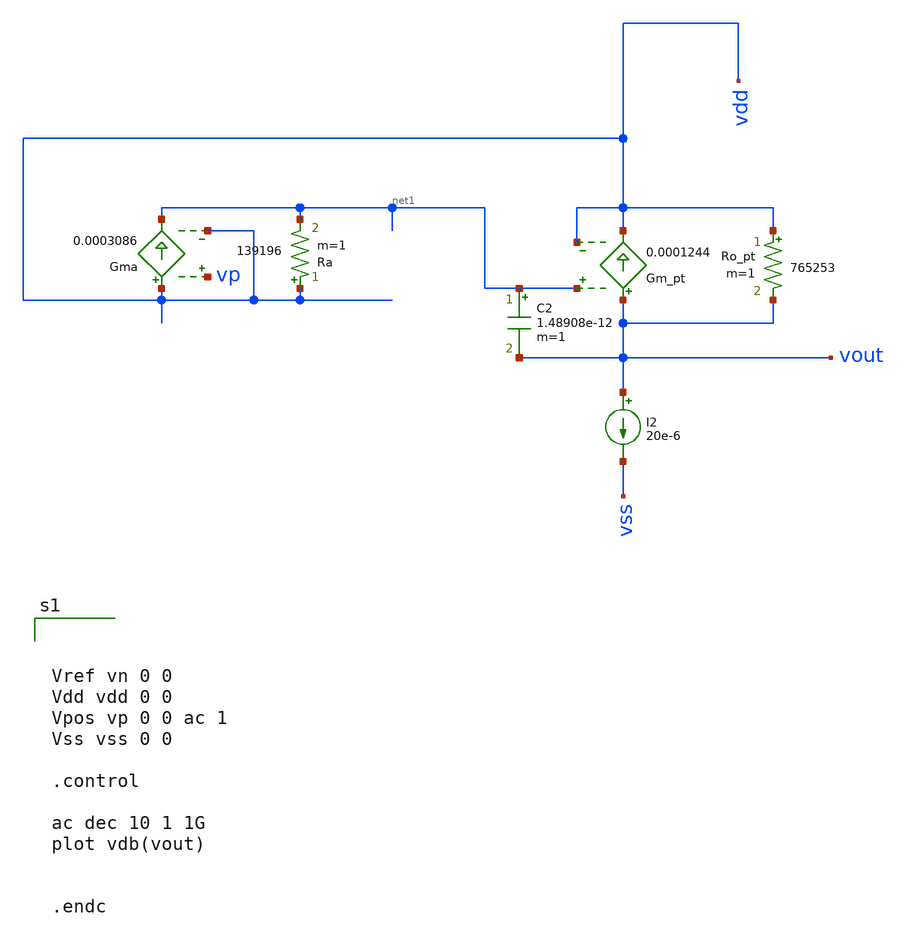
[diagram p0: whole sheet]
** sch_path: test/sstadex/xschem/stage2_OTA_tb.sch
**.subckt stage2_OTA_tb
Ro_pt vdd vout 765253 m=1
Gm_pt vout vdd net1 vdd 0.0001244
Gma vdd net1 vp vdd 0.0003086
Ra vdd net1 139196 m=1
I2 vout vss 20e-6
C2 net1 vout 1.48908e-12 m=1
**** begin user architecture code



Vref vn 0 0
Vdd vdd 0 0
Vpos vp 0 0 ac 1
Vss vss 0 0

.control

ac dec 10 1 1G
plot vdb(vout)


.endc



**** end user architecture code
**.ends
.end
